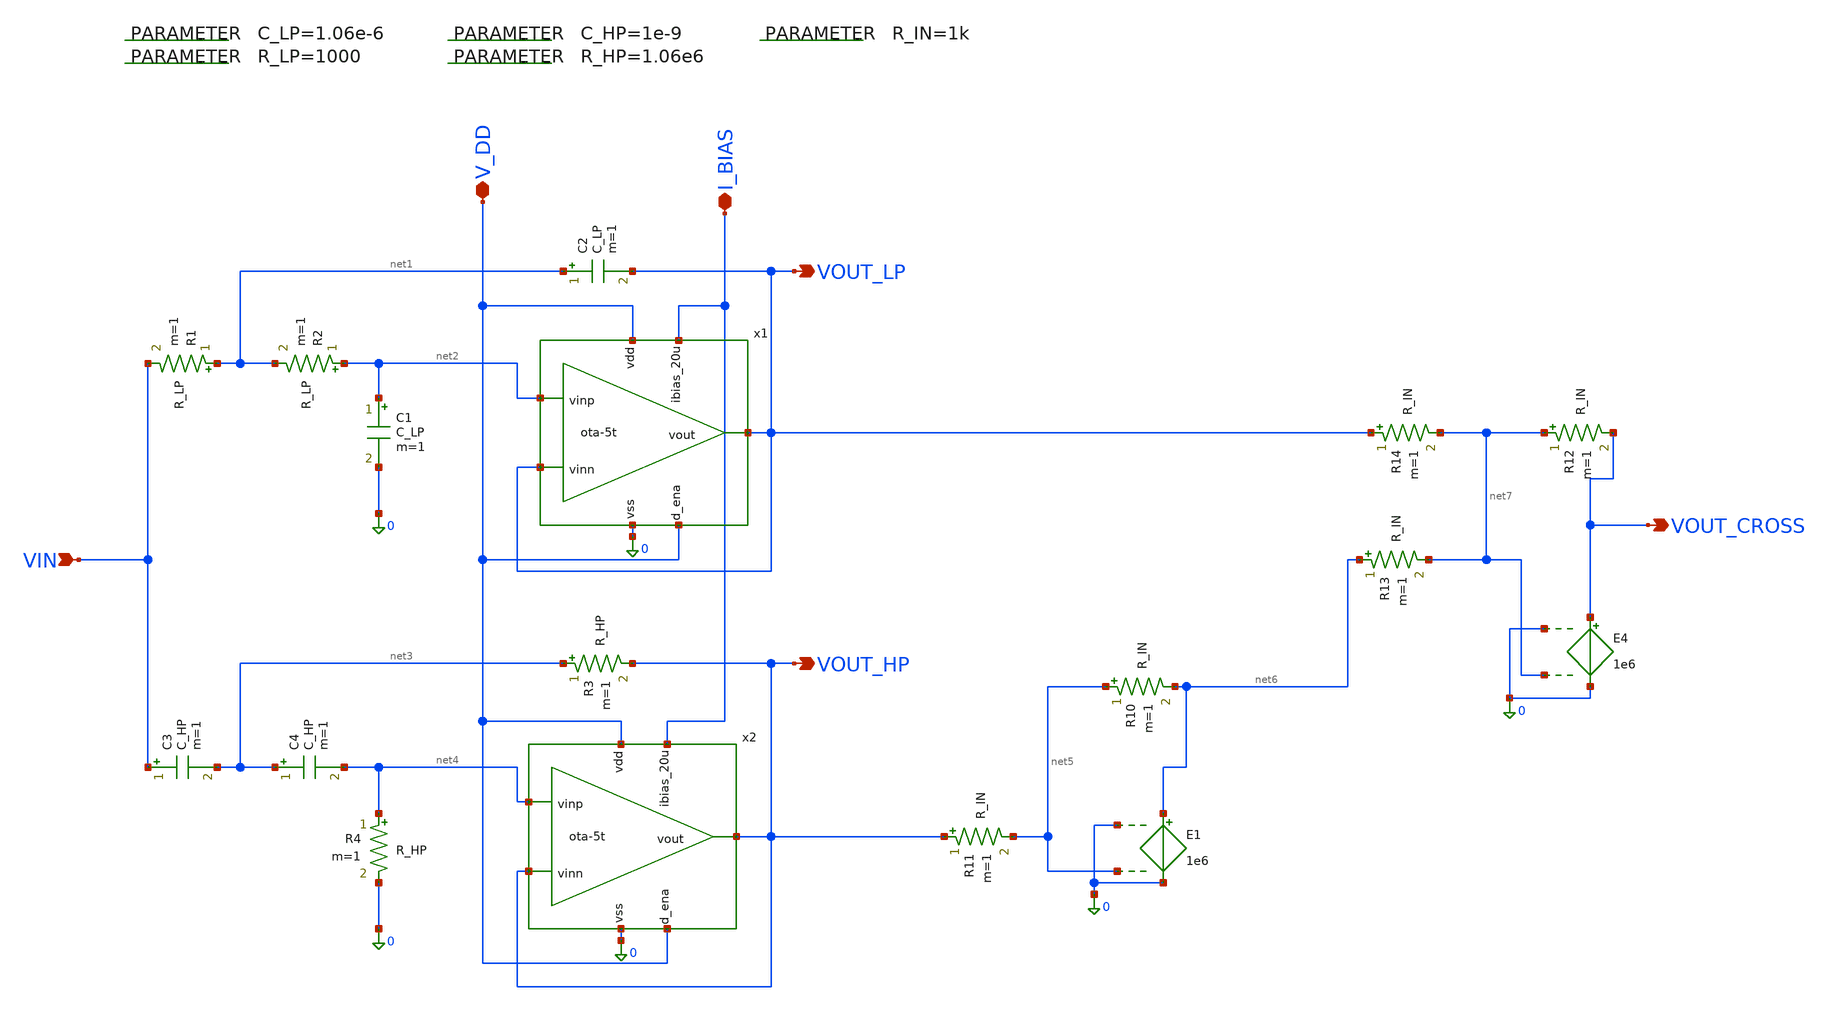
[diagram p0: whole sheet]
** sch_path: 004_Real_Circuits/linkwtz_riley_crossover_pretl_OTA.sch
* 004_Real_Circuits/ota-5t.sch:
* (c) 2024-2025 Harald Pretl, Apache-2.0 license
**.subckt linkwtz_riley_crossover_pretl_OTA VOUT_LP VOUT_HP VIN I_BIAS V_DD VOUT_CROSS
*.opin VOUT_LP
*.opin VOUT_HP
*.ipin VIN
*.iopin I_BIAS
*.iopin V_DD
*.opin VOUT_CROSS
R1 net1 VIN R_LP m=1
.param C_LP=1.06e-6
.param R_LP=1000
.param C_HP=1e-9
.param R_HP=1.06e6
.param R_IN=1k
R2 net2 net1 R_LP m=1
C1 net2 0 C_LP m=1
C2 net1 VOUT_LP C_LP m=1
C3 VIN net3 C_HP m=1
C4 net3 net4 C_HP m=1
R3 net3 VOUT_HP R_HP m=1
R4 net4 0 R_HP m=1
R10 net5 net6 R_IN m=1
R11 VOUT_HP net5 R_IN m=1
R12 net7 VOUT_CROSS R_IN m=1
R13 net6 net7 R_IN m=1
R14 VOUT_LP net7 R_IN m=1
E1 net6 0 0 net5 1e6
E4 VOUT_CROSS 0 0 net7 1e6
x1 V_DD VOUT_LP net2 VOUT_LP I_BIAS V_DD 0 ota-5t
x2 V_DD VOUT_HP net4 VOUT_HP I_BIAS V_DD 0 ota-5t
**.ends

* expanding   symbol:  /foss/designs/GitHub_Repo/004_Real_Circuits/ota-5t.sym # of pins=7
** sym_path: /foss/designs/GitHub_Repo/004_Real_Circuits/ota-5t.sym
** sch_path: /foss/designs/GitHub_Repo/004_Real_Circuits/ota-5t.sch
.subckt ota-5t vdd vout vinp vinn ibias_20u d_ena vss
*.ipin ibias_20u
*.iopin vdd
*.iopin vss
*.ipin vinp
*.ipin vinn
*.opin vout
*.ipin d_ena
XM5 tail gate_n vss vss sg13_lv_nmos w=1.0u l=5u ng=1 m=1 mm_ok=1
XM4 vout gate_p vdd vdd sg13_lv_pmos w=2.5u l=5u ng=1 m=1 mm_ok=1
XM1 gate_p vinp tail vss sg13_lv_nmos w=2u l=5u ng=1 m=1 mm_ok=1
XM2 vout vinn tail vss sg13_lv_nmos w=2u l=5u ng=1 m=1 mm_ok=1
XM3 gate_p gate_p vdd vdd sg13_lv_pmos w=2.5u l=5u ng=1 m=1 mm_ok=1
XM6 ibias_20u gate_n vss vss sg13_lv_nmos w=6.5u l=5u ng=5 m=1 mm_ok=1
XM9 gate_n ena_n vss vss sg13_lv_nmos w=0.5u l=0.13u ng=1 m=1 mm_ok=1
XM11 gate_p ena vdd vdd sg13_lv_pmos w=1.5u l=0.13u ng=1 m=1 mm_ok=1
XM7 ena ena_n vss vss sg13_lv_nmos w=0.5u l=0.13u ng=1 m=1 mm_ok=1
XM8 ena ena_n vdd vdd sg13_lv_pmos w=1.5u l=0.13u ng=1 m=1 mm_ok=1
XM10 ibias_20u ena gate_n vss sg13_lv_nmos w=0.5u l=0.13u ng=1 m=1 mm_ok=1
XM12 ena_n d_ena vss vss sg13_lv_nmos w=0.5u l=0.13u ng=1 m=1 mm_ok=1
XM13 ena_n d_ena vdd vdd sg13_lv_pmos w=1.5u l=0.13u ng=1 m=1 mm_ok=1
.ends

.end
